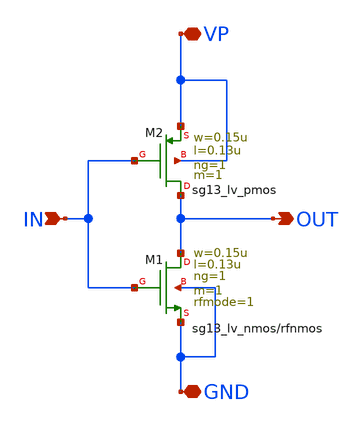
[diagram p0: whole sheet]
** sch_path: layout/inverter_test/inv_test.sch
**.subckt inv_test VP GND IN OUT
*.iopin VP
*.iopin GND
*.ipin IN
*.opin OUT
XM1 OUT IN GND GND sg13_lv_nmos w=0.15u l=0.13u ng=1 m=1 rfmode=1 mm_ok=1
XM2 OUT IN VP VP sg13_lv_pmos w=0.15u l=0.13u ng=1 m=1 mm_ok=1
**.ends
.end
